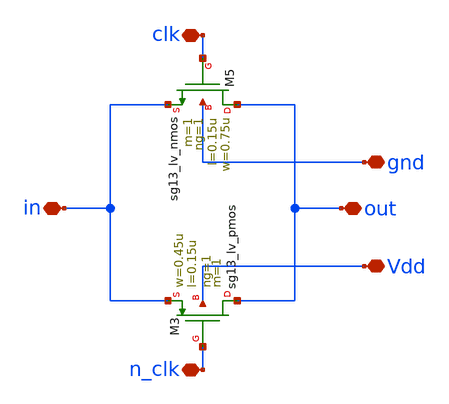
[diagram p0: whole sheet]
** sch_path: design/blocks/pgate/schematic/pgate.sch
**.subckt pgate in clk n_clk out gnd Vdd
*.iopin in
*.iopin clk
*.iopin n_clk
*.iopin out
*.iopin gnd
*.iopin Vdd
XM5 out clk in gnd sg13_lv_nmos w=0.75u l=0.15u ng=1 m=1 mm_ok=1
XM3 out n_clk in Vdd sg13_lv_pmos w=0.45u l=0.15u ng=1 m=1 mm_ok=1
**.ends
.end
